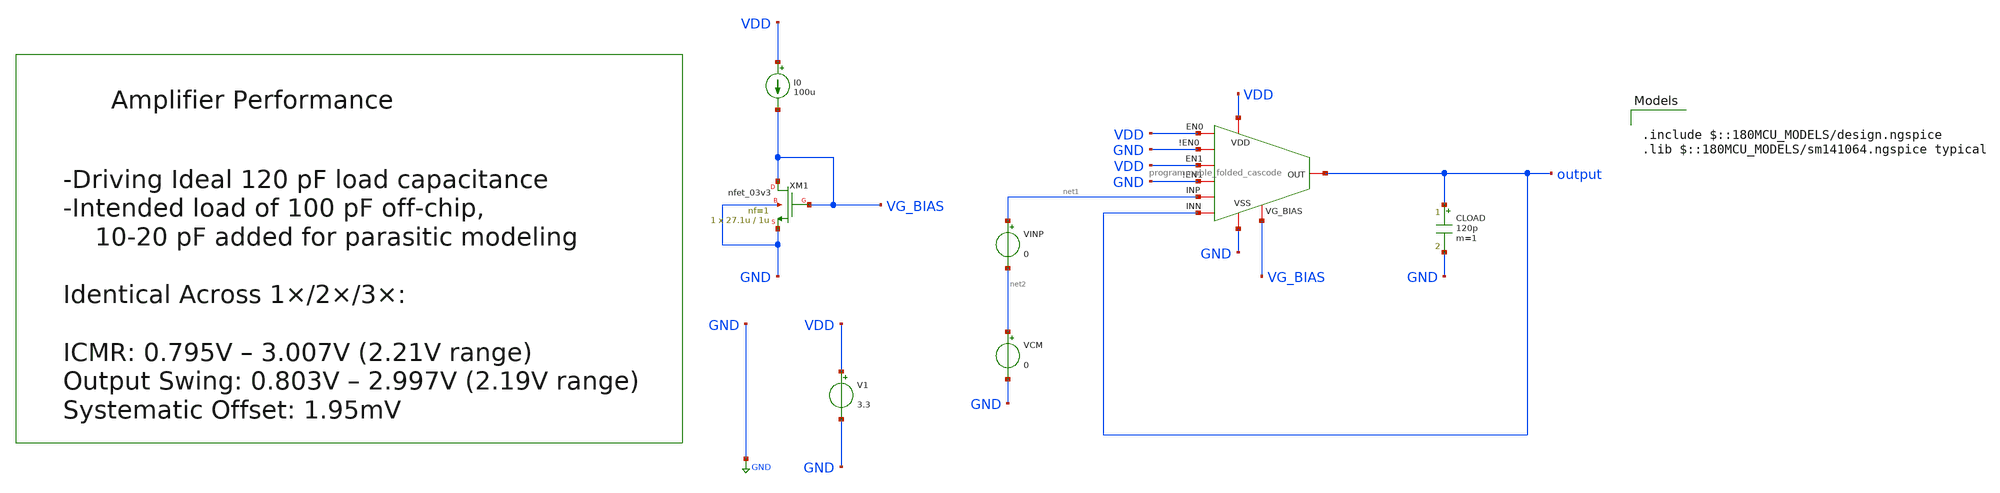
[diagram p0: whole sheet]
** sch_path: designs/libs/core_amps/ota_folded_cascode/prgram_tb/dc_unity_tb.sch
**.subckt dc_unity_tb
CLOAD output GND 120p m=1
VINP net1 net2 0
VCM net2 GND 0
x1 VDD VDD GND GND VDD GND output net1 output VG_BIAS programmable_folded_cascode
XM1 VG_BIAS VG_BIAS GND GND nfet_03v3 L=1u W=27.1u nf=1 ad='int((nf+1)/2) * W/nf * 0.18u' as='int((nf+2)/2) * W/nf * 0.18u'
+ pd='2*int((nf+1)/2) * (W/nf + 0.18u)' ps='2*int((nf+2)/2) * (W/nf + 0.18u)' nrd='0.18u / W' nrs='0.18u / W'
+ sa=0 sb=0 sd=0 m=1
I0 VDD VG_BIAS 100u
V1 VDD GND 3.3
**** begin user architecture code

.include $::180MCU_MODELS/design.ngspice
.lib $::180MCU_MODELS/sm141064.ngspice typical



.control

set color0=white
set color1=black
set color2=red
set color3=blue


dc VINP 0 4 0.001
let gain = deriv(v(output))
meas dc icmr_low when gain = 0.95 rise = 1
meas dc icmr_high when gain = 0.95 fall = 1
print icmr_low icmr_high
print icmr_high - icmr_low
meas dc out_swing_low find v(output) when gain = 0.95 rise = 1
meas dc out_swing_high find v(output) when gain = 0.95 fall = 1
print out_swing_low out_swing_high
print out_swing_high - out_swing_low
plot v(output) gain
meas dc vos find v(output) at=1.65
let offset = vos - 1.65
print offset

.endc


**** end user architecture code
**.ends

* expanding   symbol:  libs/core_amps/ota_folded_cascode/prgrm_schem/programmable_folded_cascode.sym
*+ # of pins=10
** sym_path: designs/libs/core_amps/ota_folded_cascode/prgrm_schem/programmable_folded_cascode.sym
** sch_path: designs/libs/core_amps/ota_folded_cascode/prgrm_schem/programmable_folded_cascode.sch
.subckt programmable_folded_cascode EN0 VDD !EN0 VSS EN1 !EN1 INN INP OUT VG_BIAS
*.iopin OUT
*.iopin VSS
*.iopin VDD
*.iopin EN0
*.iopin !EN0
*.iopin EN1
*.iopin !EN1
*.iopin INN
*.iopin INP
*.iopin VG_BIAS
XM29 net7 net7 VDD VDD pfet_03v3 L=1u W=23u nf=1 ad='int((nf+1)/2) * W/nf * 0.18u' as='int((nf+2)/2) * W/nf * 0.18u'
+ pd='2*int((nf+1)/2) * (W/nf + 0.18u)' ps='2*int((nf+2)/2) * (W/nf + 0.18u)' nrd='0.18u / W' nrs='0.18u / W'
+ sa=0 sb=0 sd=0 m=5
XM30 VBP2 VBP2 net7 VDD pfet_03v3 L=.5u W=19.6u nf=1 ad='int((nf+1)/2) * W/nf * 0.18u' as='int((nf+2)/2) * W/nf * 0.18u'
+ pd='2*int((nf+1)/2) * (W/nf + 0.18u)' ps='2*int((nf+2)/2) * (W/nf + 0.18u)' nrd='0.18u / W' nrs='0.18u / W'
+ sa=0 sb=0 sd=0 m=10
XM31 VBP2 VG_BIAS VSS VSS nfet_03v3 L=1u W=27.1u nf=1 ad='int((nf+1)/2) * W/nf * 0.18u' as='int((nf+2)/2) * W/nf * 0.18u'
+ pd='2*int((nf+1)/2) * (W/nf + 0.18u)' ps='2*int((nf+2)/2) * (W/nf + 0.18u)' nrd='0.18u / W' nrs='0.18u / W'
+ sa=0 sb=0 sd=0 m=1
XM32 VBN1 VBN1 VSS VSS nfet_03v3 L=1u W=27.1u nf=1 ad='int((nf+1)/2) * W/nf * 0.18u' as='int((nf+2)/2) * W/nf * 0.18u'
+ pd='2*int((nf+1)/2) * (W/nf + 0.18u)' ps='2*int((nf+2)/2) * (W/nf + 0.18u)' nrd='0.18u / W' nrs='0.18u / W'
+ sa=0 sb=0 sd=0 m=1
XM33 VBN1 net7 VDD VDD pfet_03v3 L=1u W=23u nf=1 ad='int((nf+1)/2) * W/nf * 0.18u' as='int((nf+2)/2) * W/nf * 0.18u'
+ pd='2*int((nf+1)/2) * (W/nf + 0.18u)' ps='2*int((nf+2)/2) * (W/nf + 0.18u)' nrd='0.18u / W' nrs='0.18u / W'
+ sa=0 sb=0 sd=0 m=5
XM34 VBP1 VBP1 VDD VDD pfet_03v3 L=1u W=23u nf=1 ad='int((nf+1)/2) * W/nf * 0.18u' as='int((nf+2)/2) * W/nf * 0.18u'
+ pd='2*int((nf+1)/2) * (W/nf + 0.18u)' ps='2*int((nf+2)/2) * (W/nf + 0.18u)' nrd='0.18u / W' nrs='0.18u / W'
+ sa=0 sb=0 sd=0 m=5
XM35 VBP1 VG_BIAS VSS VSS nfet_03v3 L=1u W=27.1u nf=1 ad='int((nf+1)/2) * W/nf * 0.18u' as='int((nf+2)/2) * W/nf * 0.18u'
+ pd='2*int((nf+1)/2) * (W/nf + 0.18u)' ps='2*int((nf+2)/2) * (W/nf + 0.18u)' nrd='0.18u / W' nrs='0.18u / W'
+ sa=0 sb=0 sd=0 m=1
x1 net1 VSS VBN1 VSS !EN0 VDD !EN1 EN0 EN1 VSS programmable_nfet width=20u length=1u nf=1 mult=2
x2 net2 VSS INN net1 !EN0 VDD !EN1 EN0 EN1 VSS programmable_nfet width=30u length=0.5u nf=1 mult=2
x3 net3 VSS INP net1 !EN0 VDD !EN1 EN0 EN1 VSS programmable_nfet width=30u length=0.5u nf=1 mult=2
x4 net5 VSS net5 VSS !EN0 VDD !EN1 EN0 EN1 VSS programmable_nfet width=20.5u length=1u nf=1 mult=1
x5 net6 VSS net5 VSS !EN0 VDD !EN1 EN0 EN1 VSS programmable_nfet width=20.5u length=1u nf=1 mult=1
x6 net4 VSS net4 net5 !EN0 VDD !EN1 EN0 EN1 VSS programmable_nfet width=10.5u length=0.5u nf=1
+ mult=1
x7 OUT VSS net4 net6 !EN0 VDD !EN1 EN0 EN1 VSS programmable_nfet width=10.5u length=0.5u nf=1 mult=1
x8 net4 VDD VBP2 net3 !EN0 VDD !EN1 EN0 EN1 VSS programmable_pfet width=29.6u length=0.5u nf=1
+ mult=5
x9 OUT VDD VBP2 net2 !EN0 VDD !EN1 EN0 EN1 VSS programmable_pfet width=29.6u length=0.5u nf=1 mult=5
x10 net3 VDD VBP1 VDD !EN0 VDD !EN1 EN0 EN1 VSS programmable_pfet width=34.8u length=1u nf=1 mult=10
x11 net2 VDD VBP1 VDD !EN0 VDD !EN1 EN0 EN1 VSS programmable_pfet width=34.8u length=1u nf=1 mult=10
.ends


* expanding   symbol:  libs/core_digital/schem/programmable_nfet.sym # of pins=10
** sym_path: designs/libs/core_digital/schem/programmable_nfet.sym
** sch_path: designs/libs/core_digital/schem/programmable_nfet.sch
.subckt programmable_nfet d b g s ena_bar<0> VDD ena_bar<1> ena<0> ena<1> VSS  width=0.22u
+ length=0.28u nf=1 mult=1
*.ipin VSS
*.ipin VDD
*.ipin g
*.ipin ena_bar<1>
*.ipin ena_bar<0>
*.ipin ena<1>
*.ipin ena<0>
*.iopin d
*.iopin s
*.ipin b
XM1 d net2 s b nfet_03v3 L={length} W={width} nf={nf} ad='int((nf+1)/2) * W/nf * 0.18u' as='int((nf+2)/2) * W/nf * 0.18u'
+ pd='2*int((nf+1)/2) * (W/nf + 0.18u)' ps='2*int((nf+2)/2) * (W/nf + 0.18u)' nrd='0.18u / W' nrs='0.18u / W'
+ sa=0 sb=0 sd=0 m={mult}
XM3 d net1 s b nfet_03v3 L={length} W={2*width} nf={2*nf} ad='int((nf+1)/2) * W/nf * 0.18u' as='int((nf+2)/2) * W/nf * 0.18u'
+ pd='2*int((nf+1)/2) * (W/nf + 0.18u)' ps='2*int((nf+2)/2) * (W/nf + 0.18u)' nrd='0.18u / W' nrs='0.18u / W'
+ sa=0 sb=0 sd=0 m={mult}
XM2 net1 ena_bar<1> VSS VSS nfet_03v3 L=0.28u W=0.22u nf=1 ad='int((nf+1)/2) * W/nf * 0.18u' as='int((nf+2)/2) * W/nf * 0.18u'
+ pd='2*int((nf+1)/2) * (W/nf + 0.18u)' ps='2*int((nf+2)/2) * (W/nf + 0.18u)' nrd='0.18u / W' nrs='0.18u / W'
+ sa=0 sb=0 sd=0 m=1
XM4 net2 ena_bar<0> VSS VSS nfet_03v3 L=0.28u W=0.22u nf=1 ad='int((nf+1)/2) * W/nf * 0.18u' as='int((nf+2)/2) * W/nf * 0.18u'
+ pd='2*int((nf+1)/2) * (W/nf + 0.18u)' ps='2*int((nf+2)/2) * (W/nf + 0.18u)' nrd='0.18u / W' nrs='0.18u / W'
+ sa=0 sb=0 sd=0 m=1
x1 ena_bar<0> VDD net2 g VSS ena<0> transmission_gate
x2 ena_bar<1> VDD net1 g VSS ena<1> transmission_gate
.ends


* expanding   symbol:  libs/core_digital/schem/programmable_pfet.sym # of pins=10
** sym_path: designs/libs/core_digital/schem/programmable_pfet.sym
** sch_path: designs/libs/core_digital/schem/programmable_pfet.sch
.subckt programmable_pfet d b g s ena_bar<0> VDD ena_bar<1> ena<0> ena<1> VSS  width=0.22u
+ length=0.28u nf=1 mult=1
*.ipin VSS
*.ipin VDD
*.ipin g
*.ipin ena_bar<1>
*.ipin ena_bar<0>
*.ipin ena<0>
*.iopin s
*.iopin d
*.ipin b
*.ipin ena<1>
XM1 d net2 s b pfet_03v3 L={length} W={width} nf={nf} ad='int((nf+1)/2) * W/nf * 0.18u' as='int((nf+2)/2) * W/nf * 0.18u'
+ pd='2*int((nf+1)/2) * (W/nf + 0.18u)' ps='2*int((nf+2)/2) * (W/nf + 0.18u)' nrd='0.18u / W' nrs='0.18u / W'
+ sa=0 sb=0 sd=0 m={mult}
XM3 d net1 s b pfet_03v3 L={length} W={2*width} nf={2*nf} ad='int((nf+1)/2) * W/nf * 0.18u' as='int((nf+2)/2) * W/nf * 0.18u'
+ pd='2*int((nf+1)/2) * (W/nf + 0.18u)' ps='2*int((nf+2)/2) * (W/nf + 0.18u)' nrd='0.18u / W' nrs='0.18u / W'
+ sa=0 sb=0 sd=0 m={mult}
XM2 net1 ena<1> VDD VDD pfet_03v3 L=0.28u W=0.22u nf=1 ad='int((nf+1)/2) * W/nf * 0.18u' as='int((nf+2)/2) * W/nf * 0.18u'
+ pd='2*int((nf+1)/2) * (W/nf + 0.18u)' ps='2*int((nf+2)/2) * (W/nf + 0.18u)' nrd='0.18u / W' nrs='0.18u / W'
+ sa=0 sb=0 sd=0 m=1
XM4 net2 ena<0> VDD VDD pfet_03v3 L=0.28u W=0.22u nf=1 ad='int((nf+1)/2) * W/nf * 0.18u' as='int((nf+2)/2) * W/nf * 0.18u'
+ pd='2*int((nf+1)/2) * (W/nf + 0.18u)' ps='2*int((nf+2)/2) * (W/nf + 0.18u)' nrd='0.18u / W' nrs='0.18u / W'
+ sa=0 sb=0 sd=0 m=1
x1 ena_bar<0> VDD net2 g VSS ena<0> transmission_gate
x2 ena_bar<1> VDD net1 g VSS ena<1> transmission_gate
.ends


* expanding   symbol:  libs/core_digital/schem/transmission_gate.sym # of pins=6
** sym_path: designs/libs/core_digital/schem/transmission_gate.sym
** sch_path: designs/libs/core_digital/schem/transmission_gate.sch
.subckt transmission_gate ena_bar VDD out in VSS ena
*.ipin in
*.ipin ena_bar
*.ipin ena
*.ipin VSS
*.ipin VDD
*.opin out
XM1 in ena_bar out VDD pfet_03v3 L=0.28u W=0.22u nf=1 ad='int((nf+1)/2) * W/nf * 0.18u' as='int((nf+2)/2) * W/nf * 0.18u'
+ pd='2*int((nf+1)/2) * (W/nf + 0.18u)' ps='2*int((nf+2)/2) * (W/nf + 0.18u)' nrd='0.18u / W' nrs='0.18u / W'
+ sa=0 sb=0 sd=0 m=1
XM2 in ena out VSS nfet_03v3 L=0.28u W=0.22u nf=1 ad='int((nf+1)/2) * W/nf * 0.18u' as='int((nf+2)/2) * W/nf * 0.18u'
+ pd='2*int((nf+1)/2) * (W/nf + 0.18u)' ps='2*int((nf+2)/2) * (W/nf + 0.18u)' nrd='0.18u / W' nrs='0.18u / W'
+ sa=0 sb=0 sd=0 m=1
.ends

.GLOBAL GND
.end
